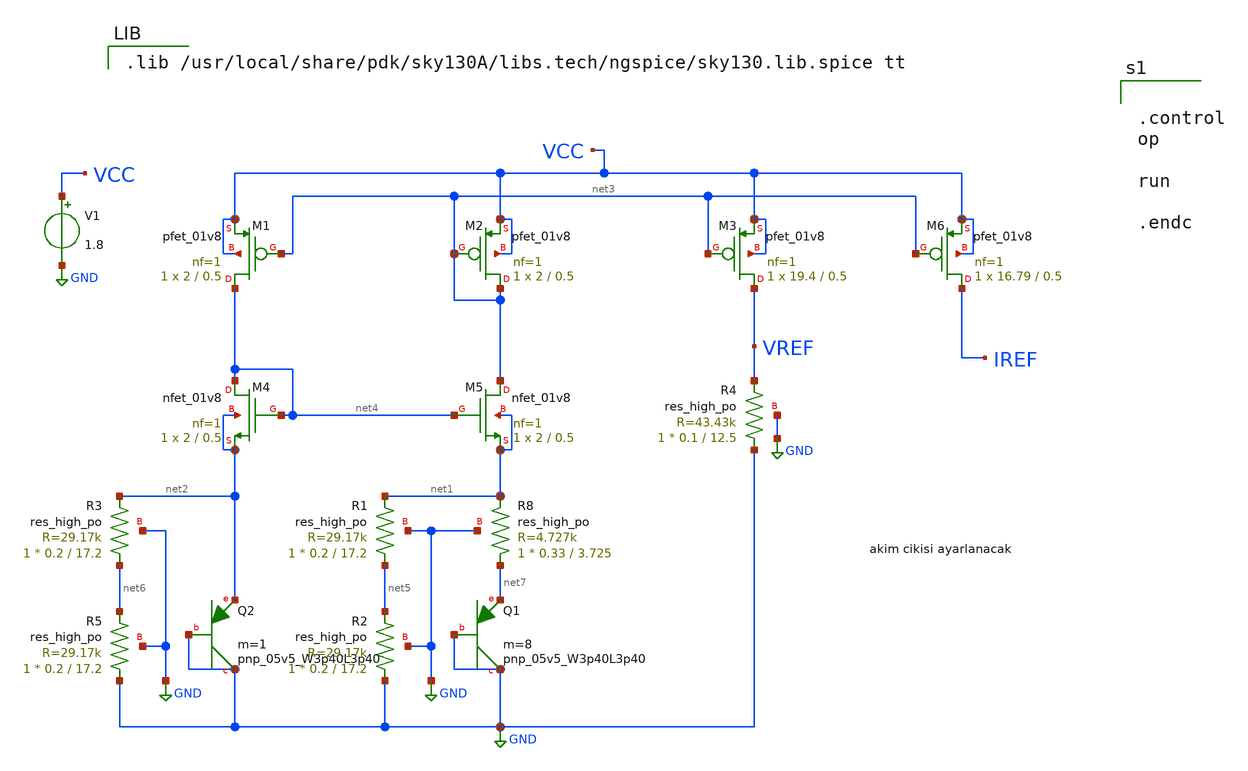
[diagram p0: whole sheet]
** sch_path: ANALOG_FOPID_XSCHEM/BGR.sch
**.subckt BGR
XM1 net4 net3 VCC VCC sky130_fd_pr__pfet_01v8 L=0.5 W=2 nf=1 ad='int((nf+1)/2) * W/nf * 0.29' as='int((nf+2)/2) * W/nf * 0.29'
+ pd='2*int((nf+1)/2) * (W/nf + 0.29)' ps='2*int((nf+2)/2) * (W/nf + 0.29)' nrd='0.29 / W' nrs='0.29 / W'
+ sa=0 sb=0 sd=0 mult=1 m=1
XM2 net3 net3 VCC VCC sky130_fd_pr__pfet_01v8 L=0.5 W=2 nf=1 ad='int((nf+1)/2) * W/nf * 0.29' as='int((nf+2)/2) * W/nf * 0.29'
+ pd='2*int((nf+1)/2) * (W/nf + 0.29)' ps='2*int((nf+2)/2) * (W/nf + 0.29)' nrd='0.29 / W' nrs='0.29 / W'
+ sa=0 sb=0 sd=0 mult=1 m=1
XM3 VREF net3 VCC VCC sky130_fd_pr__pfet_01v8 L=0.5 W=19.4 nf=1 ad='int((nf+1)/2) * W/nf * 0.29' as='int((nf+2)/2) * W/nf * 0.29'
+ pd='2*int((nf+1)/2) * (W/nf + 0.29)' ps='2*int((nf+2)/2) * (W/nf + 0.29)' nrd='0.29 / W' nrs='0.29 / W'
+ sa=0 sb=0 sd=0 mult=1 m=1
XM6 IREF net3 VCC VCC sky130_fd_pr__pfet_01v8 L=0.5 W=16.79 nf=1 ad='int((nf+1)/2) * W/nf * 0.29' as='int((nf+2)/2) * W/nf * 0.29'
+ pd='2*int((nf+1)/2) * (W/nf + 0.29)' ps='2*int((nf+2)/2) * (W/nf + 0.29)' nrd='0.29 / W' nrs='0.29 / W'
+ sa=0 sb=0 sd=0 mult=1 m=1
XQ1 GND GND net7 sky130_fd_pr__pnp_05v5_W3p40L3p40 m=8
XQ2 GND GND net2 sky130_fd_pr__pnp_05v5_W3p40L3p40 m=1
V1 VCC GND 1.8
XM5 net3 net4 net1 net1 sky130_fd_pr__nfet_01v8 L=0.5 W=2 nf=1 ad='int((nf+1)/2) * W/nf * 0.29' as='int((nf+2)/2) * W/nf * 0.29'
+ pd='2*int((nf+1)/2) * (W/nf + 0.29)' ps='2*int((nf+2)/2) * (W/nf + 0.29)' nrd='0.29 / W' nrs='0.29 / W'
+ sa=0 sb=0 sd=0 mult=1 m=1
XM4 net4 net4 net2 net2 sky130_fd_pr__nfet_01v8 L=0.5 W=2 nf=1 ad='int((nf+1)/2) * W/nf * 0.29' as='int((nf+2)/2) * W/nf * 0.29'
+ pd='2*int((nf+1)/2) * (W/nf + 0.29)' ps='2*int((nf+2)/2) * (W/nf + 0.29)' nrd='0.29 / W' nrs='0.29 / W'
+ sa=0 sb=0 sd=0 mult=1 m=1
XR8 net7 net1 GND sky130_fd_pr__res_high_po W=0.33 L=3.725 mult=1 m=1
XR1 net5 net1 GND sky130_fd_pr__res_high_po W=0.2 L=17.2 mult=1 m=1
XR2 GND net5 GND sky130_fd_pr__res_high_po W=0.2 L=17.2 mult=1 m=1
XR3 net6 net2 GND sky130_fd_pr__res_high_po W=0.2 L=17.2 mult=1 m=1
XR5 GND net6 GND sky130_fd_pr__res_high_po W=0.2 L=17.2 mult=1 m=1
XR4 GND VREF GND sky130_fd_pr__res_high_po W=0.1 L=12.5 mult=1 m=1
**** begin user architecture code

.lib /usr/local/share/pdk/sky130A/libs.tech/ngspice/sky130.lib.spice tt



.control
op

run

.endc

**** end user architecture code
**.ends
.GLOBAL GND
.end
